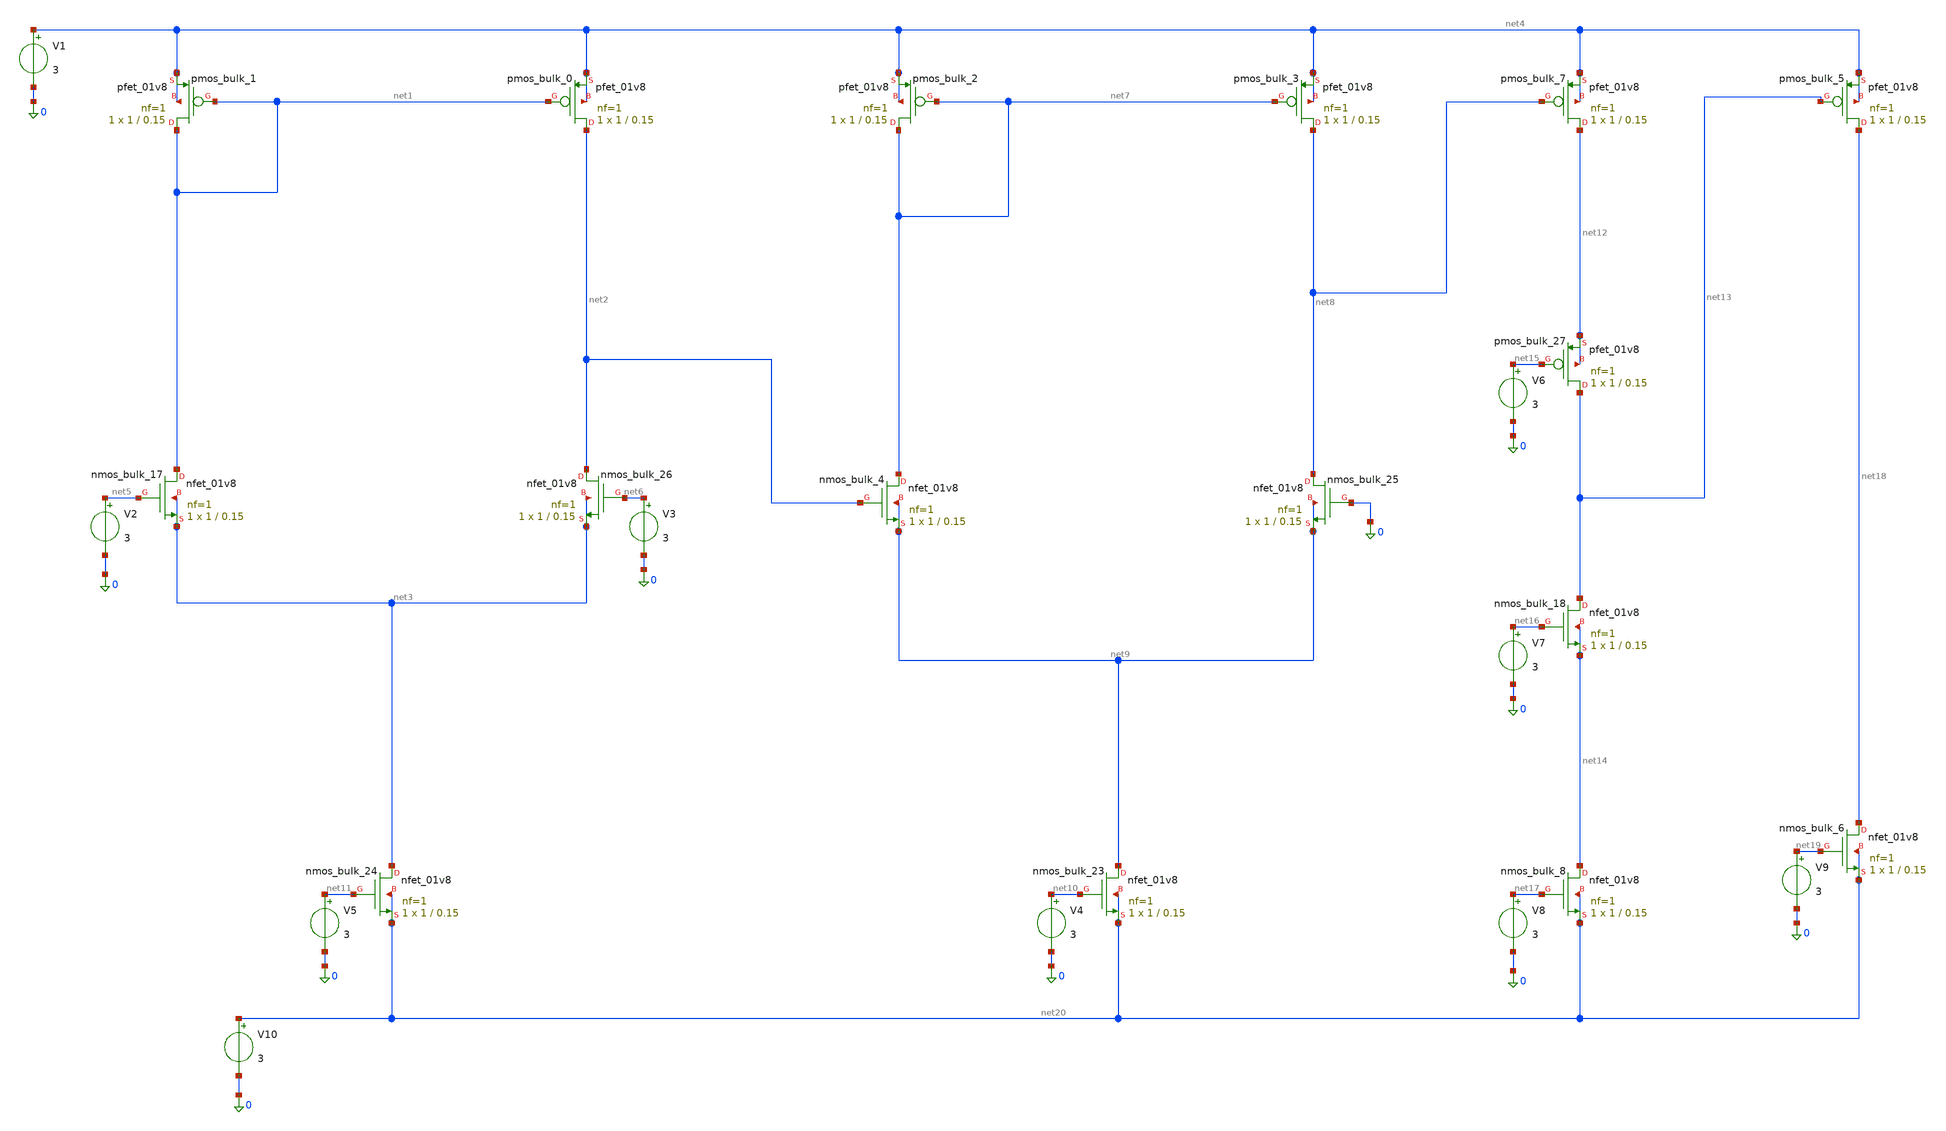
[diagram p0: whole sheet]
** sch_path: golden_netlists/10_1007_s42452-023-05572-9_11_002.sch
**.subckt 10_1007_s42452-023-05572-9_11_002
Xnmos_bulk_17 net1 net5 net3 net3 sky130_fd_pr__nfet_01v8 L=0.15 W=1 nf=1 ad='int((1 + 1)/2) * 1 / 1 * 0.29'
+ as='int((1 + 2)/2) * 1 / 1 * 0.29' pd='2*int((1 + 1)/2) * (1 / 1 + 0.29)' ps='2*int((1 + 2)/2) * (1 / 1 + 0.29)'
+ nrd='0.29 / 1 ' nrs='0.29 / 1 ' sa=0 sb=0 sd=0 mult=1 m=1
Xnmos_bulk_18 net13 net16 net14 net14 sky130_fd_pr__nfet_01v8 L=0.15 W=1 nf=1 ad='int((1 + 1)/2) * 1 / 1 * 0.29'
+ as='int((1 + 2)/2) * 1 / 1 * 0.29' pd='2*int((1 + 1)/2) * (1 / 1 + 0.29)' ps='2*int((1 + 2)/2) * (1 / 1 + 0.29)'
+ nrd='0.29 / 1 ' nrs='0.29 / 1 ' sa=0 sb=0 sd=0 mult=1 m=1
Xnmos_bulk_23 net9 net10 net20 net20 sky130_fd_pr__nfet_01v8 L=0.15 W=1 nf=1 ad='int((1 + 1)/2) * 1 / 1 * 0.29'
+ as='int((1 + 2)/2) * 1 / 1 * 0.29' pd='2*int((1 + 1)/2) * (1 / 1 + 0.29)' ps='2*int((1 + 2)/2) * (1 / 1 + 0.29)'
+ nrd='0.29 / 1 ' nrs='0.29 / 1 ' sa=0 sb=0 sd=0 mult=1 m=1
Xnmos_bulk_24 net3 net11 net20 net20 sky130_fd_pr__nfet_01v8 L=0.15 W=1 nf=1 ad='int((1 + 1)/2) * 1 / 1 * 0.29'
+ as='int((1 + 2)/2) * 1 / 1 * 0.29' pd='2*int((1 + 1)/2) * (1 / 1 + 0.29)' ps='2*int((1 + 2)/2) * (1 / 1 + 0.29)'
+ nrd='0.29 / 1 ' nrs='0.29 / 1 ' sa=0 sb=0 sd=0 mult=1 m=1
Xnmos_bulk_25 net8 0 net9 net9 sky130_fd_pr__nfet_01v8 L=0.15 W=1 nf=1 ad='int((1 + 1)/2) * 1 / 1 * 0.29'
+ as='int((1 + 2)/2) * 1 / 1 * 0.29' pd='2*int((1 + 1)/2) * (1 / 1 + 0.29)' ps='2*int((1 + 2)/2) * (1 / 1 + 0.29)'
+ nrd='0.29 / 1 ' nrs='0.29 / 1 ' sa=0 sb=0 sd=0 mult=1 m=1
Xnmos_bulk_26 net2 net6 net3 net3 sky130_fd_pr__nfet_01v8 L=0.15 W=1 nf=1 ad='int((1 + 1)/2) * 1 / 1 * 0.29'
+ as='int((1 + 2)/2) * 1 / 1 * 0.29' pd='2*int((1 + 1)/2) * (1 / 1 + 0.29)' ps='2*int((1 + 2)/2) * (1 / 1 + 0.29)'
+ nrd='0.29 / 1 ' nrs='0.29 / 1 ' sa=0 sb=0 sd=0 mult=1 m=1
Xnmos_bulk_4 net7 net2 net9 net9 sky130_fd_pr__nfet_01v8 L=0.15 W=1 nf=1 ad='int((1 + 1)/2) * 1 / 1 * 0.29'
+ as='int((1 + 2)/2) * 1 / 1 * 0.29' pd='2*int((1 + 1)/2) * (1 / 1 + 0.29)' ps='2*int((1 + 2)/2) * (1 / 1 + 0.29)'
+ nrd='0.29 / 1 ' nrs='0.29 / 1 ' sa=0 sb=0 sd=0 mult=1 m=1
Xnmos_bulk_6 net18 net19 net20 net20 sky130_fd_pr__nfet_01v8 L=0.15 W=1 nf=1 ad='int((1 + 1)/2) * 1 / 1 * 0.29'
+ as='int((1 + 2)/2) * 1 / 1 * 0.29' pd='2*int((1 + 1)/2) * (1 / 1 + 0.29)' ps='2*int((1 + 2)/2) * (1 / 1 + 0.29)'
+ nrd='0.29 / 1 ' nrs='0.29 / 1 ' sa=0 sb=0 sd=0 mult=1 m=1
Xnmos_bulk_8 net14 net17 net20 net20 sky130_fd_pr__nfet_01v8 L=0.15 W=1 nf=1 ad='int((1 + 1)/2) * 1 / 1 * 0.29'
+ as='int((1 + 2)/2) * 1 / 1 * 0.29' pd='2*int((1 + 1)/2) * (1 / 1 + 0.29)' ps='2*int((1 + 2)/2) * (1 / 1 + 0.29)'
+ nrd='0.29 / 1 ' nrs='0.29 / 1 ' sa=0 sb=0 sd=0 mult=1 m=1
Xpmos_bulk_0 net2 net1 net4 net4 sky130_fd_pr__pfet_01v8 L=0.15 W=1 nf=1 ad='int((nf+1)/2) * W/nf * 0.29'
+ as='int((nf+2)/2) * W/nf * 0.29' pd='2*int((nf+1)/2) * (W/nf + 0.29)' ps='2*int((nf+2)/2) * (W/nf + 0.29)'
+ nrd='0.29 / W' nrs='0.29 / W' sa=0 sb=0 sd=0 mult=1 m=1
Xpmos_bulk_1 net1 net1 net4 net4 sky130_fd_pr__pfet_01v8 L=0.15 W=1 nf=1 ad='int((nf+1)/2) * W/nf * 0.29'
+ as='int((nf+2)/2) * W/nf * 0.29' pd='2*int((nf+1)/2) * (W/nf + 0.29)' ps='2*int((nf+2)/2) * (W/nf + 0.29)'
+ nrd='0.29 / W' nrs='0.29 / W' sa=0 sb=0 sd=0 mult=1 m=1
Xpmos_bulk_2 net7 net7 net4 net4 sky130_fd_pr__pfet_01v8 L=0.15 W=1 nf=1 ad='int((nf+1)/2) * W/nf * 0.29'
+ as='int((nf+2)/2) * W/nf * 0.29' pd='2*int((nf+1)/2) * (W/nf + 0.29)' ps='2*int((nf+2)/2) * (W/nf + 0.29)'
+ nrd='0.29 / W' nrs='0.29 / W' sa=0 sb=0 sd=0 mult=1 m=1
Xpmos_bulk_27 net13 net15 net12 net12 sky130_fd_pr__pfet_01v8 L=0.15 W=1 nf=1 ad='int((nf+1)/2) * W/nf * 0.29'
+ as='int((nf+2)/2) * W/nf * 0.29' pd='2*int((nf+1)/2) * (W/nf + 0.29)' ps='2*int((nf+2)/2) * (W/nf + 0.29)'
+ nrd='0.29 / W' nrs='0.29 / W' sa=0 sb=0 sd=0 mult=1 m=1
Xpmos_bulk_3 net8 net7 net4 net4 sky130_fd_pr__pfet_01v8 L=0.15 W=1 nf=1 ad='int((nf+1)/2) * W/nf * 0.29'
+ as='int((nf+2)/2) * W/nf * 0.29' pd='2*int((nf+1)/2) * (W/nf + 0.29)' ps='2*int((nf+2)/2) * (W/nf + 0.29)'
+ nrd='0.29 / W' nrs='0.29 / W' sa=0 sb=0 sd=0 mult=1 m=1
Xpmos_bulk_5 net18 net13 net4 net4 sky130_fd_pr__pfet_01v8 L=0.15 W=1 nf=1 ad='int((nf+1)/2) * W/nf * 0.29'
+ as='int((nf+2)/2) * W/nf * 0.29' pd='2*int((nf+1)/2) * (W/nf + 0.29)' ps='2*int((nf+2)/2) * (W/nf + 0.29)'
+ nrd='0.29 / W' nrs='0.29 / W' sa=0 sb=0 sd=0 mult=1 m=1
Xpmos_bulk_7 net12 net8 net4 net4 sky130_fd_pr__pfet_01v8 L=0.15 W=1 nf=1 ad='int((nf+1)/2) * W/nf * 0.29'
+ as='int((nf+2)/2) * W/nf * 0.29' pd='2*int((nf+1)/2) * (W/nf + 0.29)' ps='2*int((nf+2)/2) * (W/nf + 0.29)'
+ nrd='0.29 / W' nrs='0.29 / W' sa=0 sb=0 sd=0 mult=1 m=1
V1 net4 0 3
V2 net5 0 3
V3 net6 0 3
V4 net10 0 3
V5 net11 0 3
V6 net15 0 3
V7 net16 0 3
V8 net17 0 3
V9 net19 0 3
V10 net20 0 3
**.ends
.end
